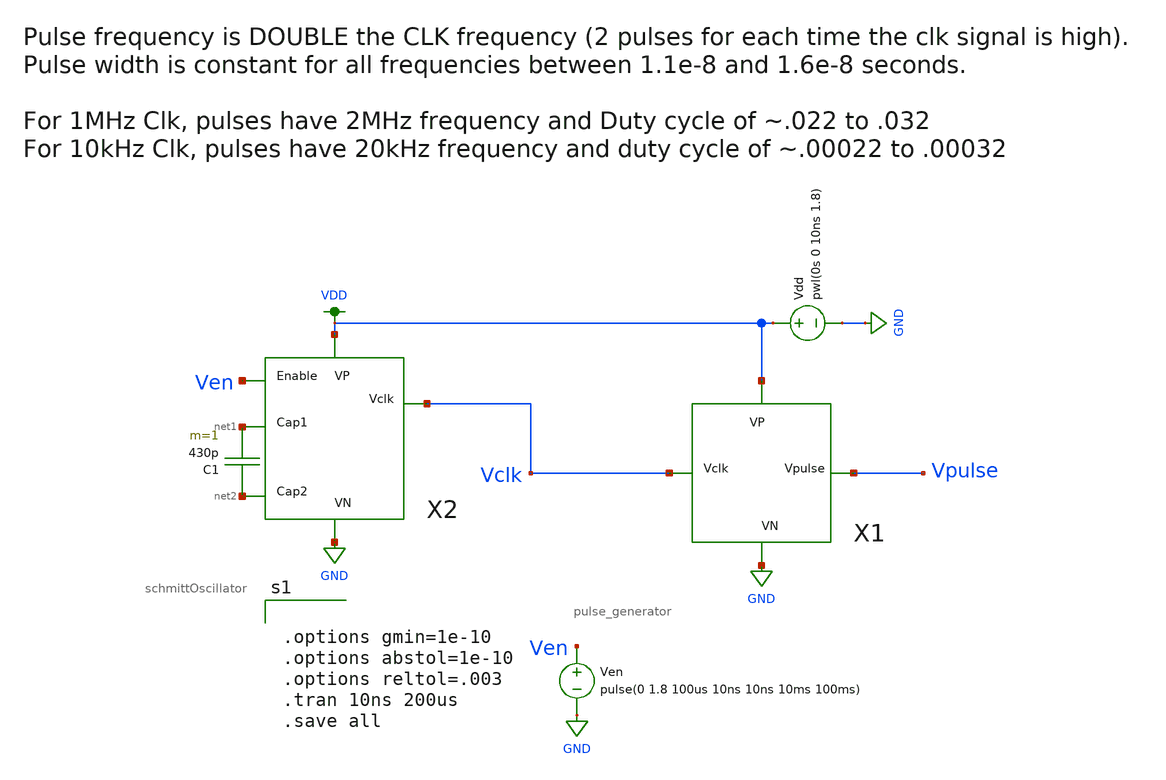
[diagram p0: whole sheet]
** sch_path: schematics/old/pulse_generator_testbench.sch
**.subckt pulse_generator_testbench
Vdd VDD GND pwl(0s 0 10ns 1.8)
X2 Ven net1 net2 VDD GND Vclk schmittOscillator
C1 net2 net1 430p m=1
X1 Vpulse VDD GND Vclk pulse_generator
Ven Ven GND pulse(0 1.8 100us 10ns 10ns 10ms 100ms)
**** begin user architecture code


.options gmin=1e-10
.options abstol=1e-10
.options reltol=.003
.tran 10ns 200us
.save all


.option wnflag=1
.lib ~/skywater/skywater-pdk/libraries/sky130_fd_pr_ngspice/latest/models/sky130.lib.spice tt

**** end user architecture code
**.ends
.GLOBAL GND
.GLOBAL VDD
.end
